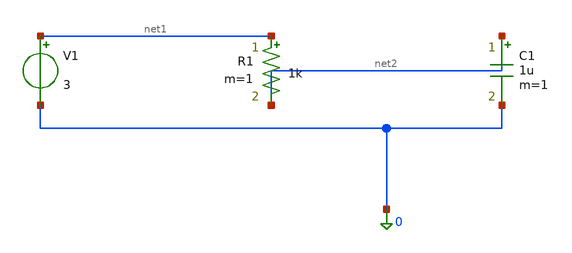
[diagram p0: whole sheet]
** sch_path: rc_circuit.sch
**.subckt rc_circuit
V1 net1 0 3
R1 net1 net2 1k m=1
C1 net2 0 1u m=1
**** begin user architecture code


.tran 100u 5m uic


**** end user architecture code
**.ends
.end
